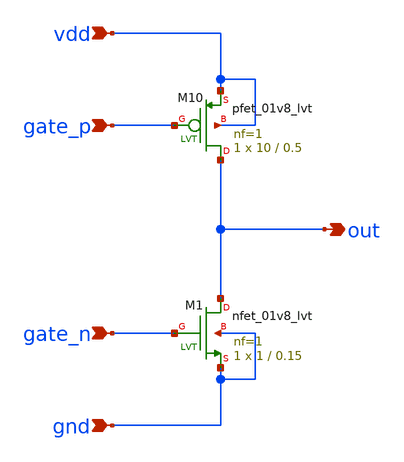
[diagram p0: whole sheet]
** sch_path: Amplifiers/simple-CS-Stage/Amp__CS-Stage.sch
**.subckt Amp__CS-Stage vdd out gnd gate_p gate_n
*.ipin vdd
*.opin out
*.ipin gnd
*.ipin gate_p
*.ipin gate_n
XM1 out gate_n gnd gnd sky130_fd_pr__nfet_01v8_lvt L=0.15 W=1 nf=1 ad='int((1 + 1)/2) * 1 / 1 * 0.29'
+ as='int((1 + 2)/2) * 1 / 1 * 0.29' pd='2*int((1 + 1)/2) * (1 / 1 + 0.29)' ps='2*int((1 + 2)/2) * (1 / 1 + 0.29)'
+ nrd='0.29 / 1 ' nrs='0.29 / 1 ' sa=0 sb=0 sd=0 mult=1 m=1
XM10 out gate_p vdd vdd sky130_fd_pr__pfet_01v8_lvt L=0.5 W=10 nf=1 ad='int((1 + 1)/2) * 10 / 1 * 0.29'
+ as='int((1 + 2)/2) * 10 / 1 * 0.29' pd='2*int((1 + 1)/2) * (10 / 1 + 0.29)' ps='2*int((1 + 2)/2) * (10 / 1 + 0.29)'
+ nrd='0.29 / 10 ' nrs='0.29 / 10 ' sa=0 sb=0 sd=0 mult=1 m=1
**.ends
.end
